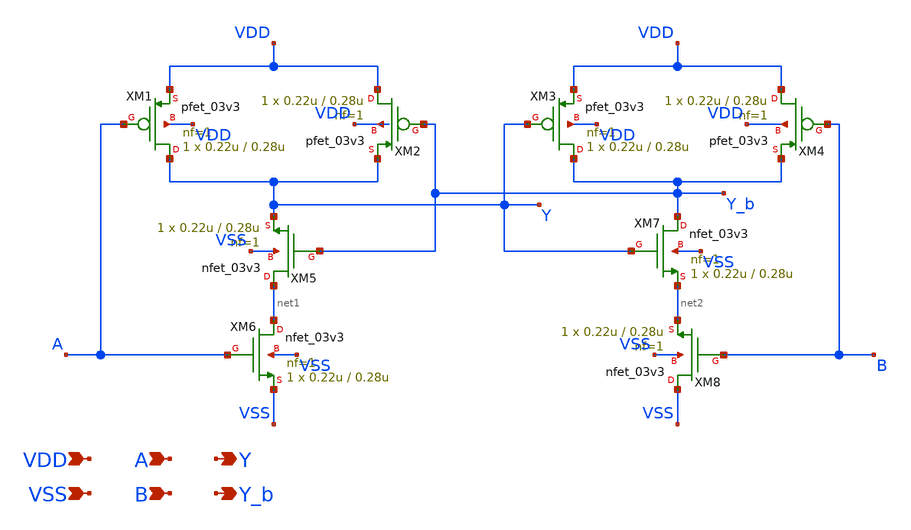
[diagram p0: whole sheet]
** sch_path: sr_latch.sch
**.subckt sr_latch VDD VSS A B Y Y_b
*.ipin VDD
*.ipin VSS
*.ipin A
*.ipin B
*.opin Y
*.opin Y_b
XM1 Y A VDD VDD pfet_03v3 L=0.28u W=0.22u nf=1 ad='int((nf+1)/2) * W/nf * 0.18u' as='int((nf+2)/2) * W/nf * 0.18u'
+ pd='2*int((nf+1)/2) * (W/nf + 0.18u)' ps='2*int((nf+2)/2) * (W/nf + 0.18u)' nrd='0.18u / W' nrs='0.18u / W'
+ sa=0 sb=0 sd=0 m=1
XM2 VDD Y_b Y VDD pfet_03v3 L=0.28u W=0.22u nf=1 ad='int((nf+1)/2) * W/nf * 0.18u' as='int((nf+2)/2) * W/nf * 0.18u'
+ pd='2*int((nf+1)/2) * (W/nf + 0.18u)' ps='2*int((nf+2)/2) * (W/nf + 0.18u)' nrd='0.18u / W' nrs='0.18u / W'
+ sa=0 sb=0 sd=0 m=1
XM5 net1 Y_b Y VSS nfet_03v3 L=0.28u W=0.22u nf=1 ad='int((nf+1)/2) * W/nf * 0.18u' as='int((nf+2)/2) * W/nf * 0.18u'
+ pd='2*int((nf+1)/2) * (W/nf + 0.18u)' ps='2*int((nf+2)/2) * (W/nf + 0.18u)' nrd='0.18u / W' nrs='0.18u / W'
+ sa=0 sb=0 sd=0 m=1
XM6 net1 A VSS VSS nfet_03v3 L=0.28u W=0.22u nf=1 ad='int((nf+1)/2) * W/nf * 0.18u' as='int((nf+2)/2) * W/nf * 0.18u'
+ pd='2*int((nf+1)/2) * (W/nf + 0.18u)' ps='2*int((nf+2)/2) * (W/nf + 0.18u)' nrd='0.18u / W' nrs='0.18u / W'
+ sa=0 sb=0 sd=0 m=1
XM3 Y_b Y VDD VDD pfet_03v3 L=0.28u W=0.22u nf=1 ad='int((nf+1)/2) * W/nf * 0.18u' as='int((nf+2)/2) * W/nf * 0.18u'
+ pd='2*int((nf+1)/2) * (W/nf + 0.18u)' ps='2*int((nf+2)/2) * (W/nf + 0.18u)' nrd='0.18u / W' nrs='0.18u / W'
+ sa=0 sb=0 sd=0 m=1
XM4 VDD B Y_b VDD pfet_03v3 L=0.28u W=0.22u nf=1 ad='int((nf+1)/2) * W/nf * 0.18u' as='int((nf+2)/2) * W/nf * 0.18u'
+ pd='2*int((nf+1)/2) * (W/nf + 0.18u)' ps='2*int((nf+2)/2) * (W/nf + 0.18u)' nrd='0.18u / W' nrs='0.18u / W'
+ sa=0 sb=0 sd=0 m=1
XM7 Y_b Y net2 VSS nfet_03v3 L=0.28u W=0.22u nf=1 ad='int((nf+1)/2) * W/nf * 0.18u' as='int((nf+2)/2) * W/nf * 0.18u'
+ pd='2*int((nf+1)/2) * (W/nf + 0.18u)' ps='2*int((nf+2)/2) * (W/nf + 0.18u)' nrd='0.18u / W' nrs='0.18u / W'
+ sa=0 sb=0 sd=0 m=1
XM8 VSS B net2 VSS nfet_03v3 L=0.28u W=0.22u nf=1 ad='int((nf+1)/2) * W/nf * 0.18u' as='int((nf+2)/2) * W/nf * 0.18u'
+ pd='2*int((nf+1)/2) * (W/nf + 0.18u)' ps='2*int((nf+2)/2) * (W/nf + 0.18u)' nrd='0.18u / W' nrs='0.18u / W'
+ sa=0 sb=0 sd=0 m=1
**.ends
.end
